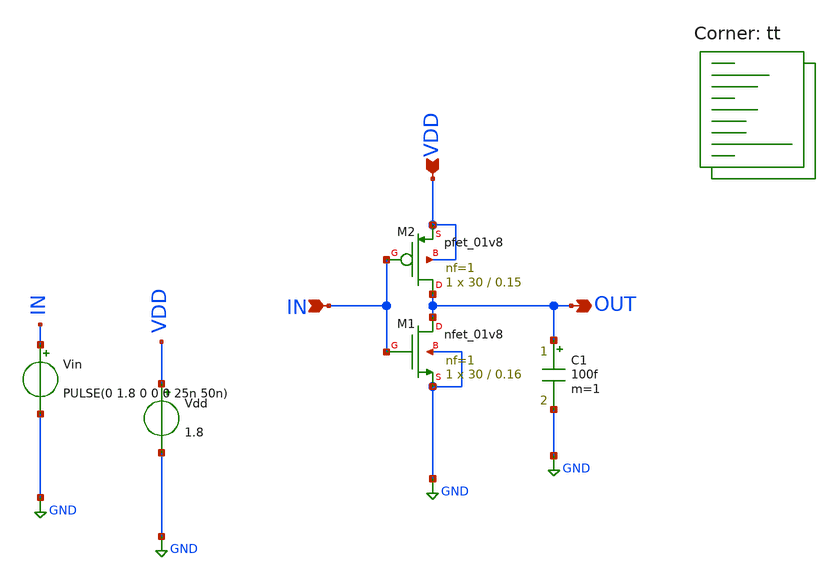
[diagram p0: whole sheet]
** sch_path: sizing-inverter.sch
**.subckt sizing-inverter IN VDD OUT
*.ipin IN
*.ipin VDD
*.opin OUT
Vin IN GND PULSE(0 1.8 0 0 0 25n 50n)
Vdd VDD GND 1.8
XM1 OUT IN GND GND sky130_fd_pr__nfet_01v8 L=0.16 W=30 nf=1 ad='int((nf+1)/2) * W/nf * 0.29' as='int((nf+2)/2) * W/nf * 0.29'
+ pd='2*int((nf+1)/2) * (W/nf + 0.29)' ps='2*int((nf+2)/2) * (W/nf + 0.29)' nrd='0.29 / W' nrs='0.29 / W'
+ sa=0 sb=0 sd=0 mult=1 m=1
XM2 OUT IN VDD VDD sky130_fd_pr__pfet_01v8 L=0.15 W=30 nf=1 ad='int((nf+1)/2) * W/nf * 0.29' as='int((nf+2)/2) * W/nf * 0.29'
+ pd='2*int((nf+1)/2) * (W/nf + 0.29)' ps='2*int((nf+2)/2) * (W/nf + 0.29)' nrd='0.29 / W' nrs='0.29 / W'
+ sa=0 sb=0 sd=0 mult=1 m=1
C1 OUT GND 100f m=1
**** begin user architecture code
.lib $::SKYWATER_MODELS/sky130.lib.spice tt


.options savecurrents

.control
save all

setplot const
let nmos_index = 0
let nmos_w = 5
let nmos_final = 30
let nmos_step = 1

let nmos_length = ceil((nmos_final - nmos_w)/nmos_step)

let pmos_initial = 20
let pmos_w = pmos_initial
let pmos_final = 80
let pmos_step = 1

let switching_points = vector(nmos_length)
let asymmetricity = vector(nmos_length)
let pmos_width = vector(nmos_length)
let nmos_width = vector(nmos_length)

while nmos_w < nmos_final

  alter m.xm1.msky130_fd_pr__nfet_01v8 W = nmos_w


  let minimum_asym = 100
  let minimum_width_pmos = 100

  let pmos_w = pmos_initial

**** Find least asymmetric pmos_w ****
  while pmos_w < pmos_final

    alter m.xm2.msky130_fd_pr__pfet_01v8 W = pmos_w
* Run transient analysis using a symmetric pulse of period 25n
    tran 10p 50n

    meas tran rise_time TRIG v(out) VAL=0.1 RISE=1 TARG v(out) VAL=1.62 RISE=1
    meas tran fall_time TRIG v(out) VAL=1.62 FALL=1 TARG v(out) VAL=0.1 FALL=1
* Create array of diffs
    let diff = abs( $&rise_time - $&fall_time )

    if diff < minimum_asym
      let minimum_asym = diff
      let minimum_width_pmos = pmos_w
    end
    print diff minimum_asym minimum_width_pmos pmos_w
    print nmos_w pmos_w
    let pmos_w = pmos_w + pmos_step
  end

  alter m.xm2.msky130_fd_pr__pfet_01v8 W = minimum_width_pmos

**** Find switching point for aforementioned pmos_w ****

  dc vin 0 1.8 1m

  meas dc switching_point WHEN v(out)=v(in) CROSS=LAST

  let switching_points[nmos_index] = $&switching_point
  let pmos_width[nmos_index] = minimum_width_pmos
  let nmos_width[nmos_index] = nmos_w
  let asymmetricity[nmos_index] = minimum_asym
  print nmos_index minimum_width_pmos

  let nmos_w = nmos_w + nmos_step
  let nmos_index = nmos_index + 1
end

plot switching_points vs nmos_width
plot pmos_width vs nmos_width
plot asymmetricity vs nmos_width

.endc


**** end user architecture code
**.ends
.GLOBAL GND
.end
